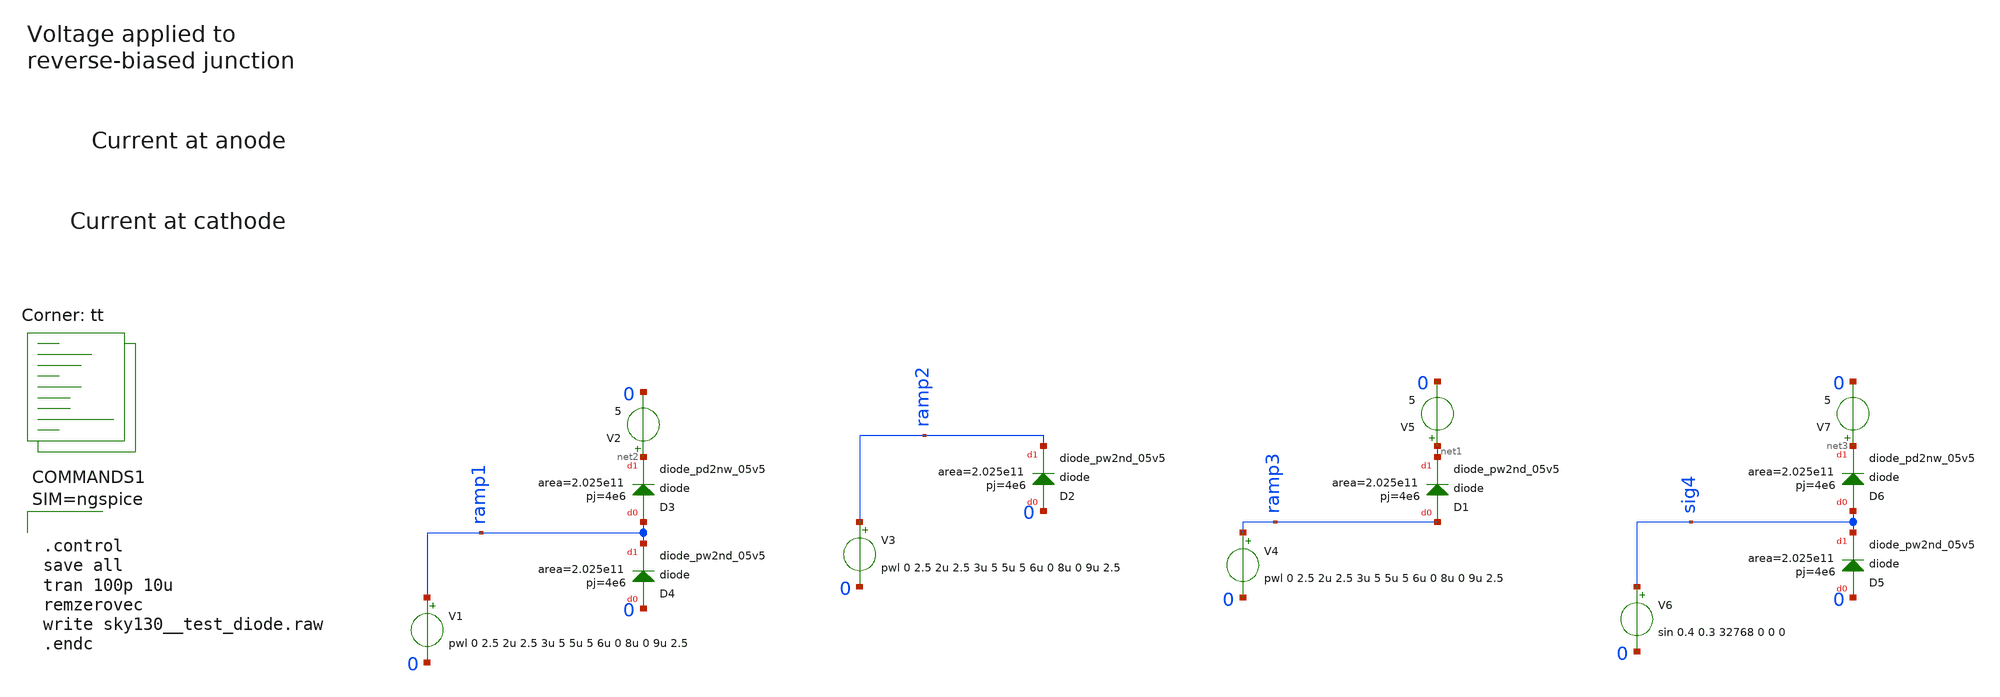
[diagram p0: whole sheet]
** sch_path: xschem/sky130__test_diode.sch
* Copyright 2021 Stefan Frederik Schippers
* Licensed under the Apache License, Version 2.0 (the "License");
* you may not use this file except in compliance with the License.
* You may obtain a copy of the License at
* https://www.apache.org/licenses/LICENSE-2.0
* Unless required by applicable law or agreed to in writing, software
* distributed under the License is distributed on an "AS IS" BASIS,
* WITHOUT WARRANTIES OR CONDITIONS OF ANY KIND, either express or implied.
* See the License for the specific language governing permissions and
* limitations under the License.
**.subckt sky130__test_diode
XD1 ramp3 net1 sky130_fd_pr__diode_pw2nd_05v5 area=2.025e11 pj=4e6
V4 ramp3 0 pwl 0 2.5 2u 2.5 3u 5 5u 5 6u 0 8u 0 9u 2.5
V5 net1 0 5
XD2 0 ramp2 sky130_fd_pr__diode_pw2nd_05v5 area=2.025e11 pj=4e6
V3 ramp2 0 pwl 0 2.5 2u 2.5 3u 5 5u 5 6u 0 8u 0 9u 2.5
XD4 0 ramp1 sky130_fd_pr__diode_pw2nd_05v5 area=2.025e11 pj=4e6
V2 net2 0 5
XD3 ramp1 net2 sky130_fd_pr__diode_pd2nw_05v5 area=2.025e11 pj=4e6
V1 ramp1 0 pwl 0 2.5 2u 2.5 3u 5 5u 5 6u 0 8u 0 9u 2.5
XD5 0 sig4 sky130_fd_pr__diode_pw2nd_05v5 area=2.025e11 pj=4e6
V7 net3 0 5
XD6 sig4 net3 sky130_fd_pr__diode_pd2nw_05v5 area=2.025e11 pj=4e6
V6 sig4 0 sin 0.4 0.3 32768 0 0 0
**** begin user architecture code



.control
save all
tran 100p 10u
remzerovec
write sky130__test_diode.raw
.endc



.lib $::SKYWATER_MODELS/sky130.lib.spice tt
**** end user architecture code
**.ends
.end
